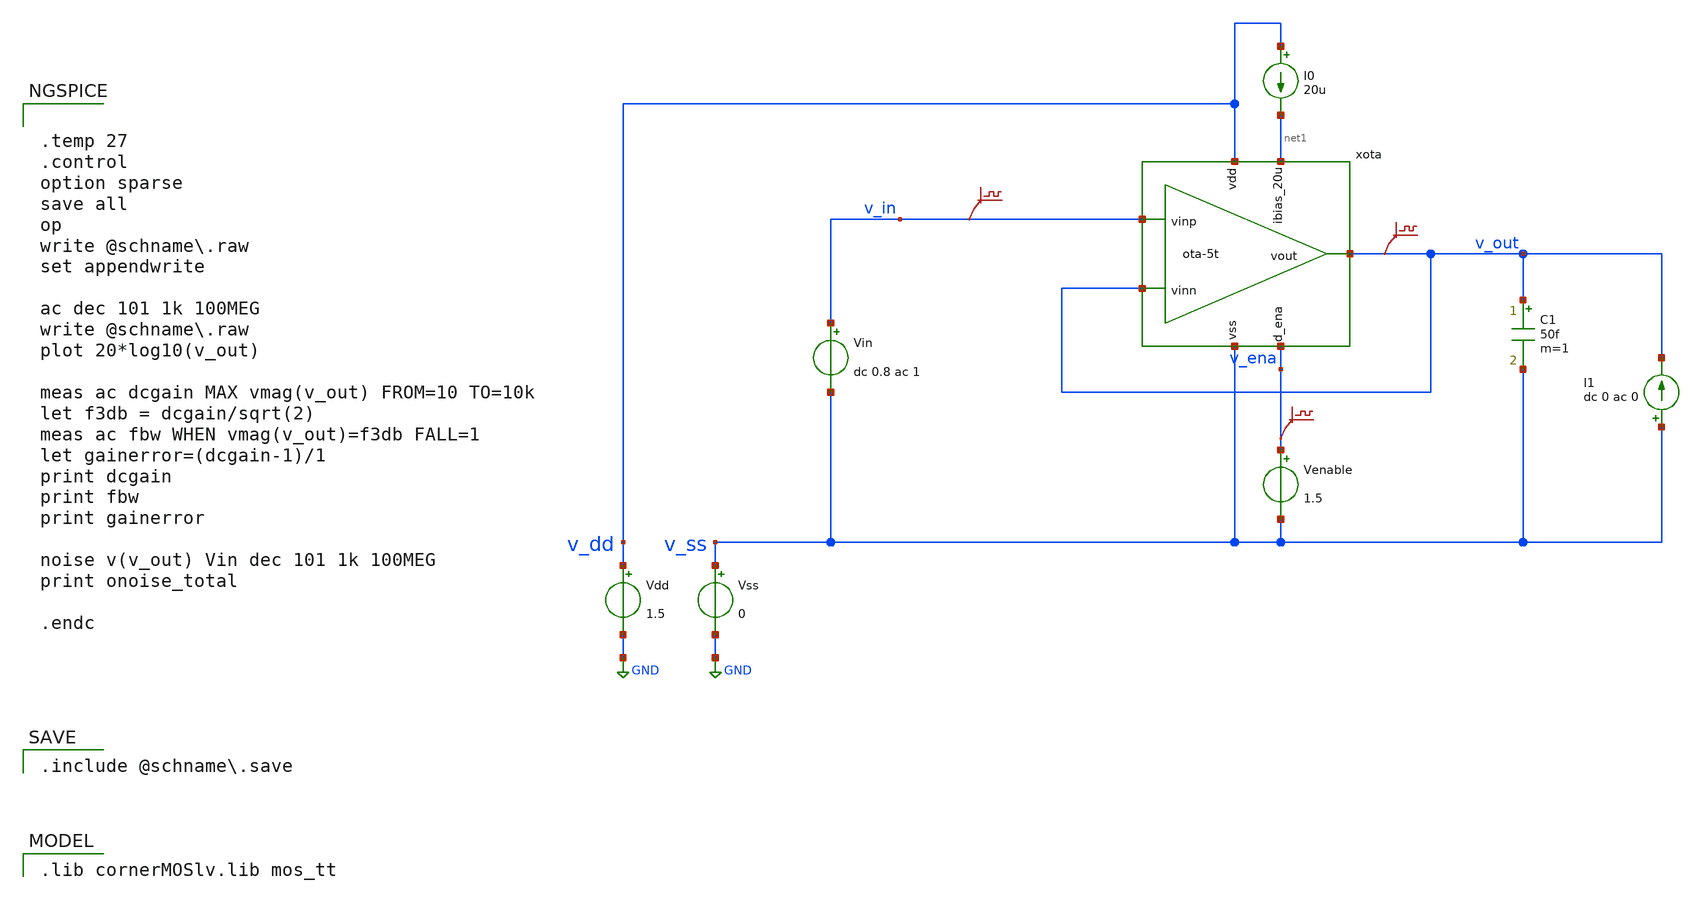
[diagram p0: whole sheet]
** sch_path: xschem/ota-5t_tb-ac.sch
* (c) 2024-2025 Harald Pretl, Apache-2.0 license
**.subckt ota-5t_tb-ac
Vdd v_dd GND 1.5
xota v_dd v_out v_in v_out net1 v_ena v_ss ota-5t
Vss v_ss GND 0
C1 v_out v_ss 50f m=1
Vin v_in v_ss dc 0.8 ac 1
I0 v_dd net1 20u
Venable v_ena v_ss 1.5
.save v(v_in)
.save v(v_out)
.save v(v_ena)
I1 v_ss v_out dc 0 ac 0
**** begin user architecture code
 .lib cornerMOSlv.lib mos_tt



.temp 27
.control
option sparse
save all
op
write @schname\.raw
set appendwrite

ac dec 101 1k 100MEG
write @schname\.raw
plot 20*log10(v_out)

meas ac dcgain MAX vmag(v_out) FROM=10 TO=10k
let f3db = dcgain/sqrt(2)
meas ac fbw WHEN vmag(v_out)=f3db FALL=1
let gainerror=(dcgain-1)/1
print dcgain
print fbw
print gainerror

noise v(v_out) Vin dec 101 1k 100MEG
print onoise_total

.endc


 .include @schname.save

**** end user architecture code
**.ends
.GLOBAL GND
.end
